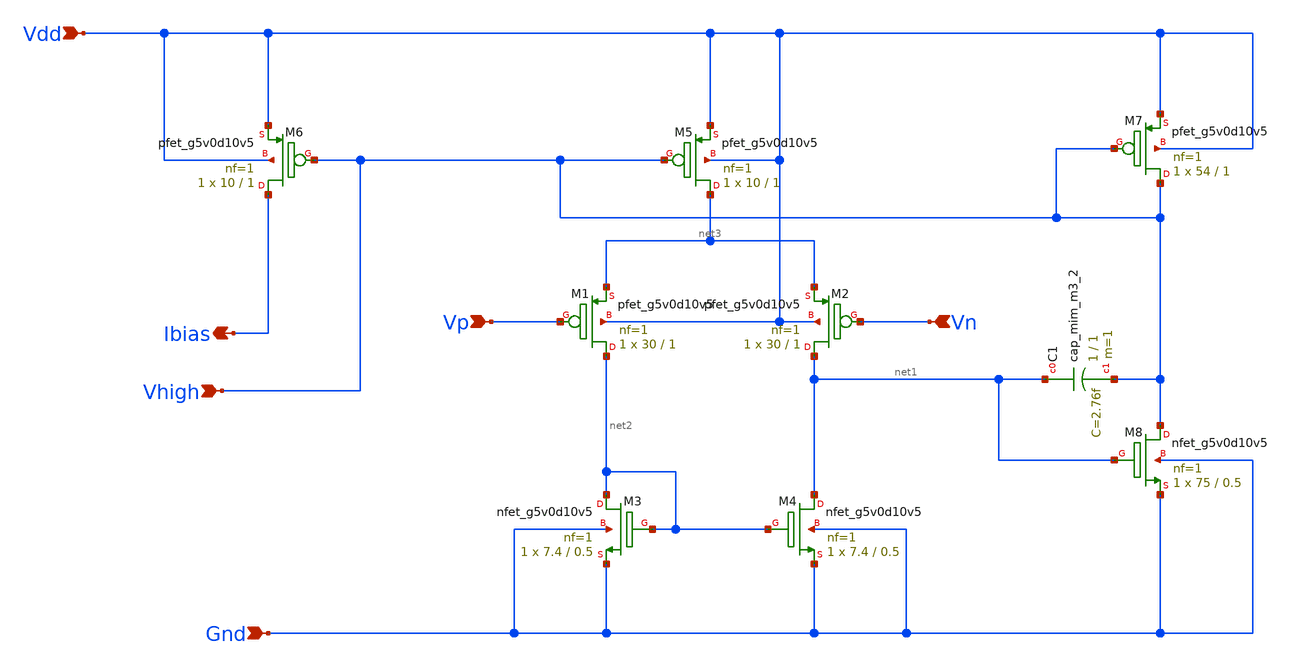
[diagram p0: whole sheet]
** sch_path: Bandgap/Schematics/BGR5v/Bandgap5v_OTA.sch
**.subckt Bandgap5v_OTA Ibias Vhigh Vdd Gnd Vn Vp
*.opin Ibias
*.ipin Vhigh
*.ipin Vdd
*.ipin Gnd
*.ipin Vn
*.ipin Vp
XM6 Ibias Vhigh Vdd Vdd sky130_fd_pr__pfet_g5v0d10v5 L=1 W=10 nf=1 ad='int((nf+1)/2) * W/nf * 0.29' as='int((nf+2)/2) * W/nf * 0.29'
+ pd='2*int((nf+1)/2) * (W/nf + 0.29)' ps='2*int((nf+2)/2) * (W/nf + 0.29)' nrd='0.29 / W' nrs='0.29 / W'
+ sa=0 sb=0 sd=0 mult=1 m=1
XM5 net3 Vhigh Vdd Vdd sky130_fd_pr__pfet_g5v0d10v5 L=1 W=10 nf=1 ad='int((nf+1)/2) * W/nf * 0.29' as='int((nf+2)/2) * W/nf * 0.29'
+ pd='2*int((nf+1)/2) * (W/nf + 0.29)' ps='2*int((nf+2)/2) * (W/nf + 0.29)' nrd='0.29 / W' nrs='0.29 / W'
+ sa=0 sb=0 sd=0 mult=1 m=1
XM7 Vhigh Vhigh Vdd Vdd sky130_fd_pr__pfet_g5v0d10v5 L=1 W=54 nf=1 ad='int((nf+1)/2) * W/nf * 0.29' as='int((nf+2)/2) * W/nf * 0.29'
+ pd='2*int((nf+1)/2) * (W/nf + 0.29)' ps='2*int((nf+2)/2) * (W/nf + 0.29)' nrd='0.29 / W' nrs='0.29 / W'
+ sa=0 sb=0 sd=0 mult=1 m=1
XM2 net1 Vn net3 Vdd sky130_fd_pr__pfet_g5v0d10v5 L=1 W=30 nf=1 ad='int((nf+1)/2) * W/nf * 0.29' as='int((nf+2)/2) * W/nf * 0.29'
+ pd='2*int((nf+1)/2) * (W/nf + 0.29)' ps='2*int((nf+2)/2) * (W/nf + 0.29)' nrd='0.29 / W' nrs='0.29 / W'
+ sa=0 sb=0 sd=0 mult=1 m=1
XM1 net2 Vp net3 Vdd sky130_fd_pr__pfet_g5v0d10v5 L=1 W=30 nf=1 ad='int((nf+1)/2) * W/nf * 0.29' as='int((nf+2)/2) * W/nf * 0.29'
+ pd='2*int((nf+1)/2) * (W/nf + 0.29)' ps='2*int((nf+2)/2) * (W/nf + 0.29)' nrd='0.29 / W' nrs='0.29 / W'
+ sa=0 sb=0 sd=0 mult=1 m=1
XM8 Vhigh net1 Gnd Gnd sky130_fd_pr__nfet_g5v0d10v5 L=0.5 W=75 nf=1 ad='int((nf+1)/2) * W/nf * 0.29'
+ as='int((nf+2)/2) * W/nf * 0.29' pd='2*int((nf+1)/2) * (W/nf + 0.29)' ps='2*int((nf+2)/2) * (W/nf + 0.29)'
+ nrd='0.29 / W' nrs='0.29 / W' sa=0 sb=0 sd=0 mult=1 m=1
XM4 net1 net2 Gnd Gnd sky130_fd_pr__nfet_g5v0d10v5 L=0.5 W=7.4 nf=1 ad='int((nf+1)/2) * W/nf * 0.29'
+ as='int((nf+2)/2) * W/nf * 0.29' pd='2*int((nf+1)/2) * (W/nf + 0.29)' ps='2*int((nf+2)/2) * (W/nf + 0.29)'
+ nrd='0.29 / W' nrs='0.29 / W' sa=0 sb=0 sd=0 mult=1 m=1
XM3 net2 net2 Gnd Gnd sky130_fd_pr__nfet_g5v0d10v5 L=0.5 W=7.4 nf=1 ad='int((nf+1)/2) * W/nf * 0.29'
+ as='int((nf+2)/2) * W/nf * 0.29' pd='2*int((nf+1)/2) * (W/nf + 0.29)' ps='2*int((nf+2)/2) * (W/nf + 0.29)'
+ nrd='0.29 / W' nrs='0.29 / W' sa=0 sb=0 sd=0 mult=1 m=1
XC1 net1 Vhigh sky130_fd_pr__cap_mim_m3_2 W=1 L=1 MF=1 m=1
**.ends
.end
